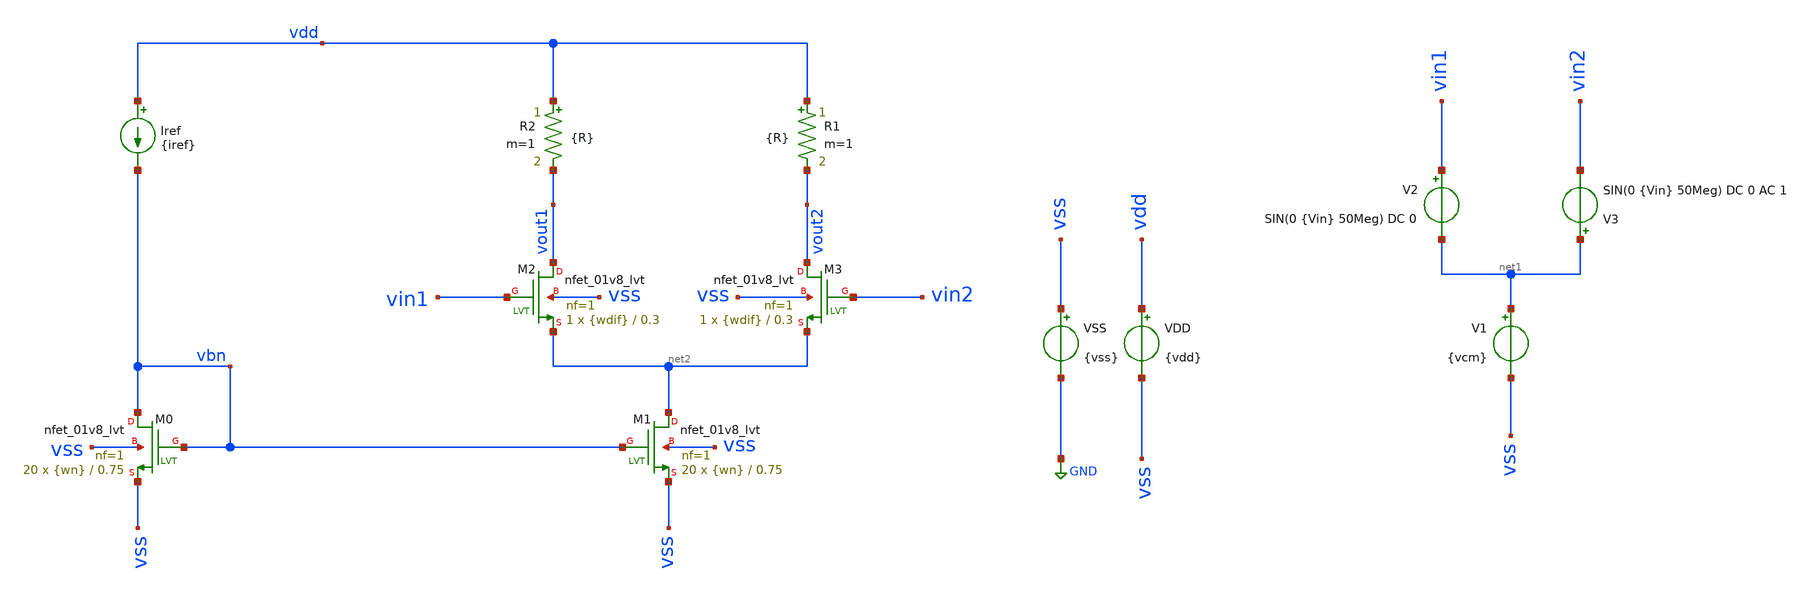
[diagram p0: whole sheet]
** sch_path: tp3/tp3_1.sch
**.subckt tp3_1
Iref vdd vbn {iref}
VSS vss GND {vss}
VDD vdd vss {vdd}
V1 net1 vss {vcm}
XM1 net2 vbn vss vss sky130_fd_pr__nfet_01v8_lvt L=0.75 W={wn} nf=1 ad='int((nf+1)/2) * W/nf * 0.29'
+ as='int((nf+2)/2) * W/nf * 0.29' pd='2*int((nf+1)/2) * (W/nf + 0.29)' ps='2*int((nf+2)/2) * (W/nf + 0.29)'
+ nrd='0.29 / W' nrs='0.29 / W' sa=0 sb=0 sd=0 mult=20 m=20
XM0 vbn vbn vss vss sky130_fd_pr__nfet_01v8_lvt L=0.75 W={wn} nf=1 ad='int((nf+1)/2) * W/nf * 0.29' as='int((nf+2)/2) * W/nf * 0.29'
+ pd='2*int((nf+1)/2) * (W/nf + 0.29)' ps='2*int((nf+2)/2) * (W/nf + 0.29)' nrd='0.29 / W' nrs='0.29 / W'
+ sa=0 sb=0 sd=0 mult=20 m=20
XM2 vout1 vin1 net2 vss sky130_fd_pr__nfet_01v8_lvt L=0.3 W={wdif} nf=1 ad='int((nf+1)/2) * W/nf * 0.29'
+ as='int((nf+2)/2) * W/nf * 0.29' pd='2*int((nf+1)/2) * (W/nf + 0.29)' ps='2*int((nf+2)/2) * (W/nf + 0.29)'
+ nrd='0.29 / W' nrs='0.29 / W' sa=0 sb=0 sd=0 mult=1 m=1
R2 vdd vout1 {R} m=1
XM3 vout2 vin2 net2 vss sky130_fd_pr__nfet_01v8_lvt L=0.3 W={wdif} nf=1 ad='int((nf+1)/2) * W/nf * 0.29'
+ as='int((nf+2)/2) * W/nf * 0.29' pd='2*int((nf+1)/2) * (W/nf + 0.29)' ps='2*int((nf+2)/2) * (W/nf + 0.29)'
+ nrd='0.29 / W' nrs='0.29 / W' sa=0 sb=0 sd=0 mult=1 m=1
R1 vdd vout2 {R} m=1
V2 vin1 net1 SIN(0 {Vin} 50Meg) DC 0
V3 net1 vin2 SIN(0 {Vin} 50Meg) DC 0 AC 1
**** begin user architecture code



* Parameters
.param vdd = 1.8
.param vss = 0.0
.param iref = 100u
.param wn = 8
.param wdif = 3.5
.param R = 12k
.param Vin = 10m
.param vcm = 1.2

.options TEMP = 65.0

* Models
*.lib ~/skywater/skywater-pdk/libraries/sky130_fd_pr_ngspice/latest/models/corners/sky130.lib TT
*.lib /foss/pdks/sky130A/libs.tech/ngspice/sky130.lib.spice tt
.lib /foss/pdks/sky130A/libs.tech/ngspice/sky130.lib.spice.tt.red tt
* Data to save
.save all  @M.XM0.msky130_fd_pr__nfet_01v8_lvt[id]  @M.XM0.msky130_fd_pr__nfet_01v8_lvt[vds]  @M.XM0.msky130_fd_pr__nfet_01v8_lvt[vgs]  @M.XM0.msky130_fd_pr__nfet_01v8_lvt[vdsat]  @M.XM0.msky130_fd_pr__nfet_01v8_lvt[vth]  @M.XM0.msky130_fd_pr__nfet_01v8_lvt[gm]  @M.XM1.msky130_fd_pr__nfet_01v8_lvt[id]  @M.XM1.msky130_fd_pr__nfet_01v8_lvt[vds]  @M.XM1.msky130_fd_pr__nfet_01v8_lvt[vgs]  @M.XM1.msky130_fd_pr__nfet_01v8_lvt[vdsat]  @M.XM1.msky130_fd_pr__nfet_01v8_lvt[vth]  @M.XM1.msky130_fd_pr__nfet_01v8_lvt[gm]  @M.XM1.msky130_fd_pr__nfet_01v8_lvt[gds]  @M.XM2.msky130_fd_pr__nfet_01v8_lvt[id]  @M.XM2.msky130_fd_pr__nfet_01v8_lvt[vds]  @M.XM2.msky130_fd_pr__nfet_01v8_lvt[vgs]  @M.XM2.msky130_fd_pr__nfet_01v8_lvt[vdsat]  @M.XM2.msky130_fd_pr__nfet_01v8_lvt[vth]  @M.XM2.msky130_fd_pr__nfet_01v8_lvt[gm]  @M.XM2.msky130_fd_pr__nfet_01v8_lvt[gds]  @M.XM3.msky130_fd_pr__nfet_01v8_lvt[id]  @M.XM3.msky130_fd_pr__nfet_01v8_lvt[vds]  @M.XM3.msky130_fd_pr__nfet_01v8_lvt[vgs]  @M.XM3.msky130_fd_pr__nfet_01v8_lvt[vdsat]  @M.XM3.msky130_fd_pr__nfet_01v8_lvt[vth]  @M.XM3.msky130_fd_pr__nfet_01v8_lvt[gm]  @M.XM3.msky130_fd_pr__nfet_01v8_lvt[gds]

* Simulation
.control


  ac dec 100 10k 100G
  let vdiff = vout1-vout2
  let vindiff = vin1-vin2
  setplot ac1
  meas ac GBW when vdb(vdiff) = 0
  meas ac DCG find vdb(vdiff) at=10k
  meas ac PM find vp(vdiff) when vdb(vdiff)=0
  print PM*180/PI
  meas ac GM find vdb(vdiff) when vp(vdiff)=0
  plot vdb(vdiff) {vp(vdiff)*180/PI}
  write tp3_1_ac.raw

  reset
  tran 0.01n 100n
  let vdiff = vout1-vout2
  let vindiff = vin1-vin2
  plot v(vindiff) v(vdiff)
 plot v(vout1) v(vout2)
 plot v(vin1) v(vin2)
  write tp3_1_tran.raw
reset
 op
  save all
  print all
  unset filetype
  write tp3_1.raw



.endc

.end


**** end user architecture code
**.ends
.GLOBAL GND
.end
